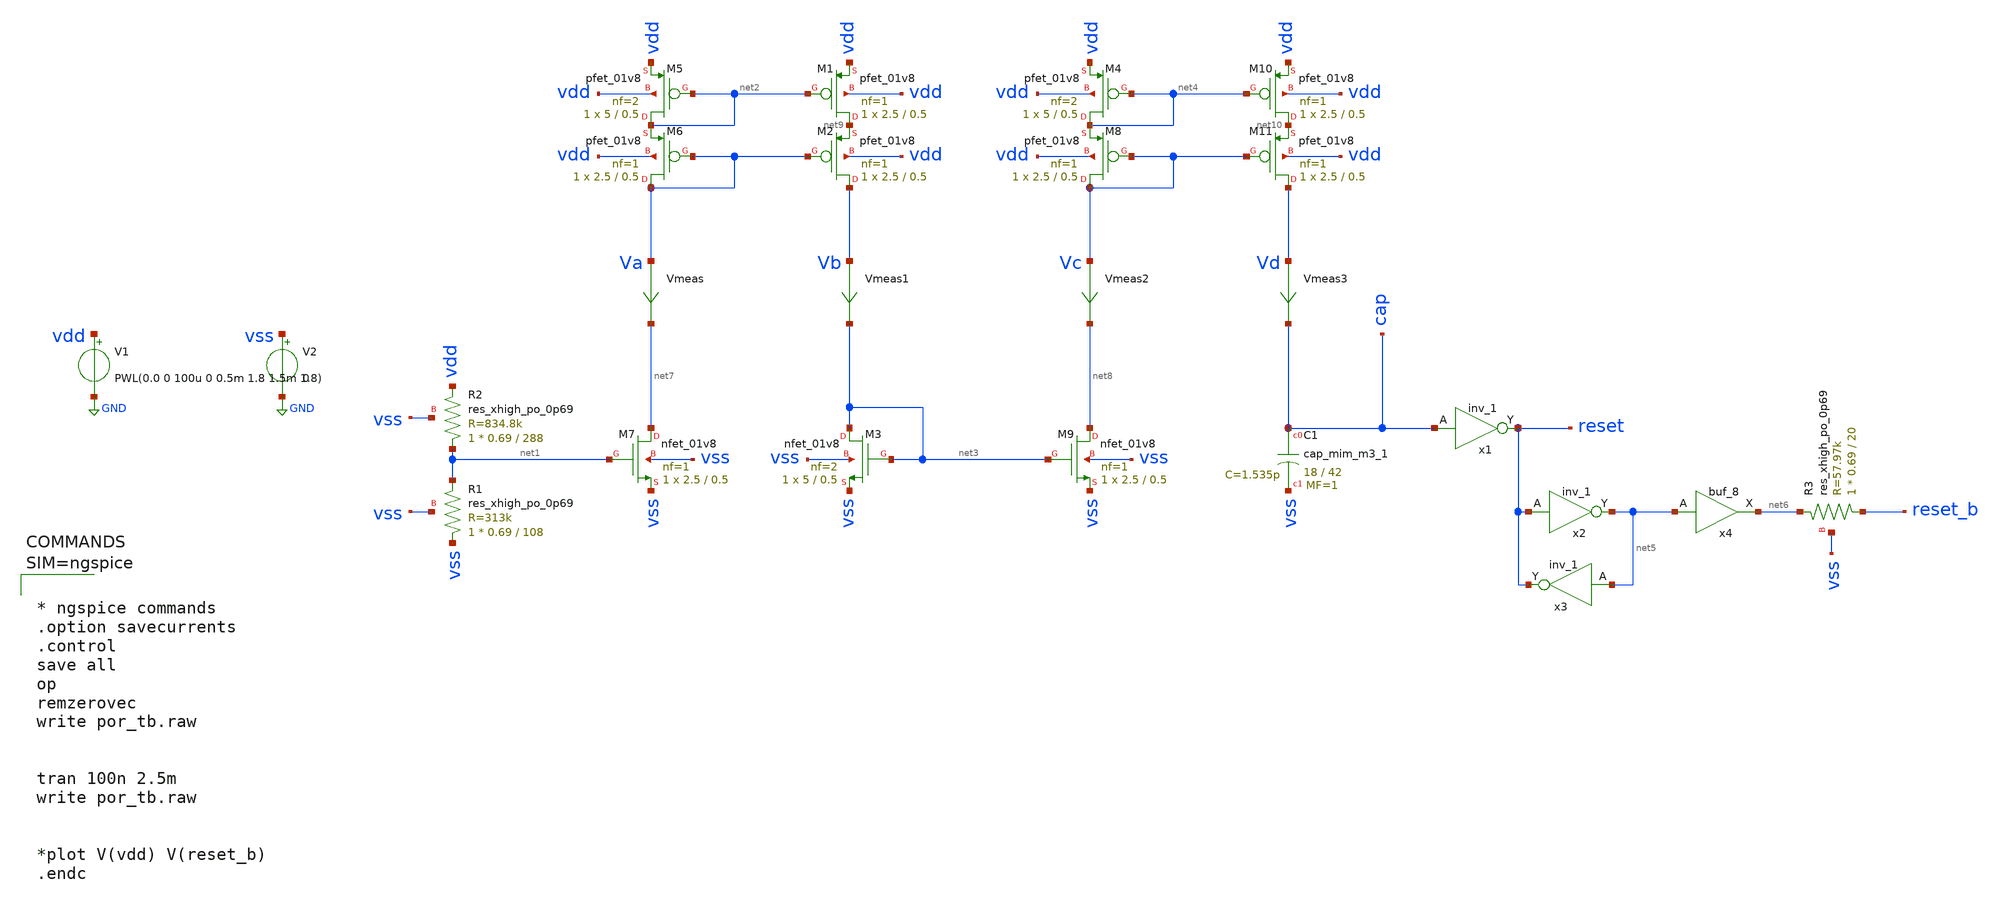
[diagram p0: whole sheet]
** sch_path: xschem/por_tb2.sch
**.subckt por_tb2
V1 vdd GND PWL(0.0 0 100u 0 0.5m 1.8 1.5m 1.8)
V2 vss GND 0
XC1 cap vss sky130_fd_pr__cap_mim_m3_1 W=18 L=42 MF=1 m=1
x1 cap vss vss vdd vdd reset sky130_fd_sc_hd__inv_1
XR1 vss net1 vss sky130_fd_pr__res_xhigh_po_0p69 L=108 mult=1 m=1
XM5 net2 net2 vdd vdd sky130_fd_pr__pfet_01v8 L=0.5 W=5 nf=2 ad='int((nf+1)/2) * W/nf * 0.29' as='int((nf+2)/2) * W/nf * 0.29'
+ pd='2*int((nf+1)/2) * (W/nf + 0.29)' ps='2*int((nf+2)/2) * (W/nf + 0.29)' nrd='0.29 / W' nrs='0.29 / W'
+ sa=0 sb=0 sd=0 mult=1 m=1
XM6 Va Va net2 vdd sky130_fd_pr__pfet_01v8 L=0.5 W=2.5 nf=1 ad='int((nf+1)/2) * W/nf * 0.29' as='int((nf+2)/2) * W/nf * 0.29'
+ pd='2*int((nf+1)/2) * (W/nf + 0.29)' ps='2*int((nf+2)/2) * (W/nf + 0.29)' nrd='0.29 / W' nrs='0.29 / W'
+ sa=0 sb=0 sd=0 mult=1 m=1
XM7 net7 net1 vss vss sky130_fd_pr__nfet_01v8 L=0.5 W=2.5 nf=1 ad='int((nf+1)/2) * W/nf * 0.29' as='int((nf+2)/2) * W/nf * 0.29'
+ pd='2*int((nf+1)/2) * (W/nf + 0.29)' ps='2*int((nf+2)/2) * (W/nf + 0.29)' nrd='0.29 / W' nrs='0.29 / W'
+ sa=0 sb=0 sd=0 mult=1 m=1
XR2 net1 vdd vss sky130_fd_pr__res_xhigh_po_0p69 L=288 mult=1 m=1
XM1 net9 net2 vdd vdd sky130_fd_pr__pfet_01v8 L=0.5 W=2.5 nf=1 ad='int((nf+1)/2) * W/nf * 0.29' as='int((nf+2)/2) * W/nf * 0.29'
+ pd='2*int((nf+1)/2) * (W/nf + 0.29)' ps='2*int((nf+2)/2) * (W/nf + 0.29)' nrd='0.29 / W' nrs='0.29 / W'
+ sa=0 sb=0 sd=0 mult=1 m=1
XM2 Vb Va net9 vdd sky130_fd_pr__pfet_01v8 L=0.5 W=2.5 nf=1 ad='int((nf+1)/2) * W/nf * 0.29' as='int((nf+2)/2) * W/nf * 0.29'
+ pd='2*int((nf+1)/2) * (W/nf + 0.29)' ps='2*int((nf+2)/2) * (W/nf + 0.29)' nrd='0.29 / W' nrs='0.29 / W'
+ sa=0 sb=0 sd=0 mult=1 m=1
XM3 net3 net3 vss vss sky130_fd_pr__nfet_01v8 L=0.5 W=5 nf=2 ad='int((nf+1)/2) * W/nf * 0.29' as='int((nf+2)/2) * W/nf * 0.29'
+ pd='2*int((nf+1)/2) * (W/nf + 0.29)' ps='2*int((nf+2)/2) * (W/nf + 0.29)' nrd='0.29 / W' nrs='0.29 / W'
+ sa=0 sb=0 sd=0 mult=1 m=1
XM4 net4 net4 vdd vdd sky130_fd_pr__pfet_01v8 L=0.5 W=5 nf=2 ad='int((nf+1)/2) * W/nf * 0.29' as='int((nf+2)/2) * W/nf * 0.29'
+ pd='2*int((nf+1)/2) * (W/nf + 0.29)' ps='2*int((nf+2)/2) * (W/nf + 0.29)' nrd='0.29 / W' nrs='0.29 / W'
+ sa=0 sb=0 sd=0 mult=1 m=1
XM8 Vc Vc net4 vdd sky130_fd_pr__pfet_01v8 L=0.5 W=2.5 nf=1 ad='int((nf+1)/2) * W/nf * 0.29' as='int((nf+2)/2) * W/nf * 0.29'
+ pd='2*int((nf+1)/2) * (W/nf + 0.29)' ps='2*int((nf+2)/2) * (W/nf + 0.29)' nrd='0.29 / W' nrs='0.29 / W'
+ sa=0 sb=0 sd=0 mult=1 m=1
XM9 net8 net3 vss vss sky130_fd_pr__nfet_01v8 L=0.5 W=2.5 nf=1 ad='int((nf+1)/2) * W/nf * 0.29' as='int((nf+2)/2) * W/nf * 0.29'
+ pd='2*int((nf+1)/2) * (W/nf + 0.29)' ps='2*int((nf+2)/2) * (W/nf + 0.29)' nrd='0.29 / W' nrs='0.29 / W'
+ sa=0 sb=0 sd=0 mult=1 m=1
XM10 net10 net4 vdd vdd sky130_fd_pr__pfet_01v8 L=0.5 W=2.5 nf=1 ad='int((nf+1)/2) * W/nf * 0.29' as='int((nf+2)/2) * W/nf * 0.29'
+ pd='2*int((nf+1)/2) * (W/nf + 0.29)' ps='2*int((nf+2)/2) * (W/nf + 0.29)' nrd='0.29 / W' nrs='0.29 / W'
+ sa=0 sb=0 sd=0 mult=1 m=1
XM11 Vd Vc net10 vdd sky130_fd_pr__pfet_01v8 L=0.5 W=2.5 nf=1 ad='int((nf+1)/2) * W/nf * 0.29' as='int((nf+2)/2) * W/nf * 0.29'
+ pd='2*int((nf+1)/2) * (W/nf + 0.29)' ps='2*int((nf+2)/2) * (W/nf + 0.29)' nrd='0.29 / W' nrs='0.29 / W'
+ sa=0 sb=0 sd=0 mult=1 m=1
x2 reset vss vss vdd vdd net5 sky130_fd_sc_hd__inv_1
x3 net5 vss vss vdd vdd reset sky130_fd_sc_hd__inv_1
x4 net5 vss vss vdd vdd net6 sky130_fd_sc_hd__buf_8
XR3 reset_b net6 vss sky130_fd_pr__res_xhigh_po_0p69 L=20 mult=1 m=1
Vmeas Va net7 0
.save i(vmeas)
Vmeas1 Vb net3 0
.save i(vmeas1)
Vmeas2 Vc net8 0
.save i(vmeas2)
Vmeas3 Vd cap 0
.save i(vmeas3)
**** begin user architecture code

** opencircuitdesign pdks install
.lib $::SKYWATER_MODELS/sky130.lib.spice tt
.include $::SKYWATER_STDCELLS/sky130_fd_sc_hd.spice




* ngspice commands
.option savecurrents
.control
save all
op
remzerovec
write por_tb.raw


tran 100n 2.5m
write por_tb.raw


*plot V(vdd) V(reset_b)
.endc



**** end user architecture code
**.ends
.GLOBAL GND
.end
